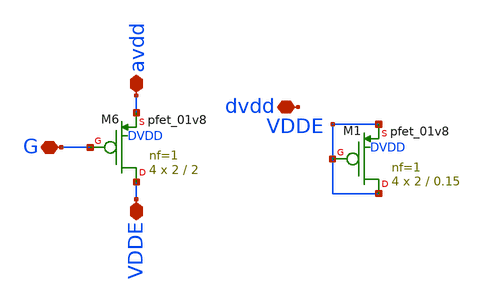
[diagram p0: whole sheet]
** sch_path: magic/pmos_ena.sch
**.subckt pmos_ena G avdd VDDE dvdd
*.iopin G
*.iopin avdd
*.iopin VDDE
*.iopin dvdd
XM6 VDDE G avdd DVDD sky130_fd_pr__pfet_01v8 L=2 W=2 nf=1 ad='int((nf+1)/2) * W/nf * 0.29' as='int((nf+2)/2) * W/nf * 0.29'
+ pd='2*int((nf+1)/2) * (W/nf + 0.29)' ps='2*int((nf+2)/2) * (W/nf + 0.29)' nrd='0.29 / W' nrs='0.29 / W'
+ sa=0 sb=0 sd=0 mult=4 m=4
XM1 VDDE VDDE VDDE DVDD sky130_fd_pr__pfet_01v8 L=0.15 W=2 nf=1 ad='int((nf+1)/2) * W/nf * 0.29' as='int((nf+2)/2) * W/nf * 0.29'
+ pd='2*int((nf+1)/2) * (W/nf + 0.29)' ps='2*int((nf+2)/2) * (W/nf + 0.29)' nrd='0.29 / W' nrs='0.29 / W'
+ sa=0 sb=0 sd=0 mult=4 m=4
**.ends
.end
